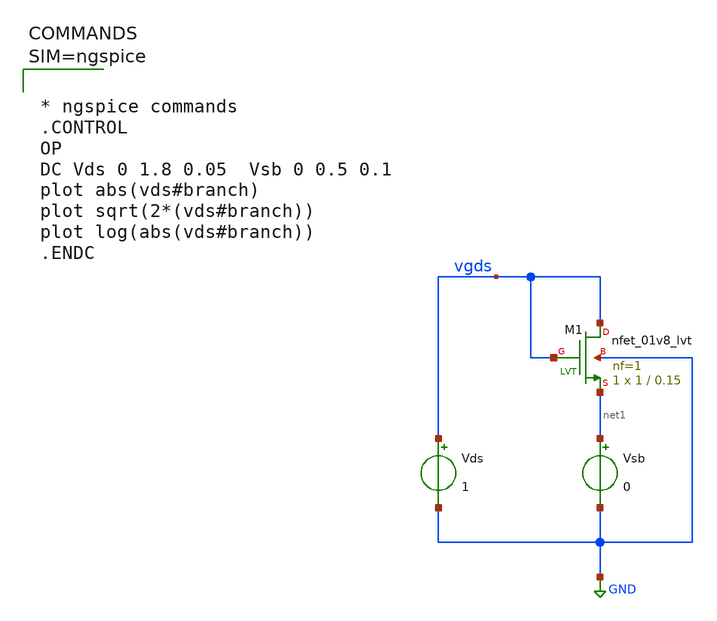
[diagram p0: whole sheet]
** sch_path: xschem/param_extract.sch
**.subckt param_extract
XM1 vgds vgds net1 GND sky130_fd_pr__nfet_01v8_lvt L=0.15 W=1 nf=1 ad='int((1 + 1)/2) * 1 / 1 * 0.29'
+ as='int((1 + 2)/2) * 1 / 1 * 0.29' pd='2*int((1 + 1)/2) * (1 / 1 + 0.29)' ps='2*int((1 + 2)/2) * (1 / 1 + 0.29)'
+ nrd='0.29 / 1 ' nrs='0.29 / 1 ' sa=0 sb=0 sd=0 mult=1 m=1
Vds vgds GND 1
Vsb net1 GND 0
**** begin user architecture code



* ngspice commands
.CONTROL
OP
DC Vds 0 1.8 0.05  Vsb 0 0.5 0.1
plot abs(vds#branch)
plot sqrt(2*(vds#branch))
plot log(abs(vds#branch))
.ENDC




** opencircuitdesign pdks install
.lib $::SKYWATER_MODELS/sky130.lib.spice tt

**** end user architecture code
**.ends
.GLOBAL GND
.end
